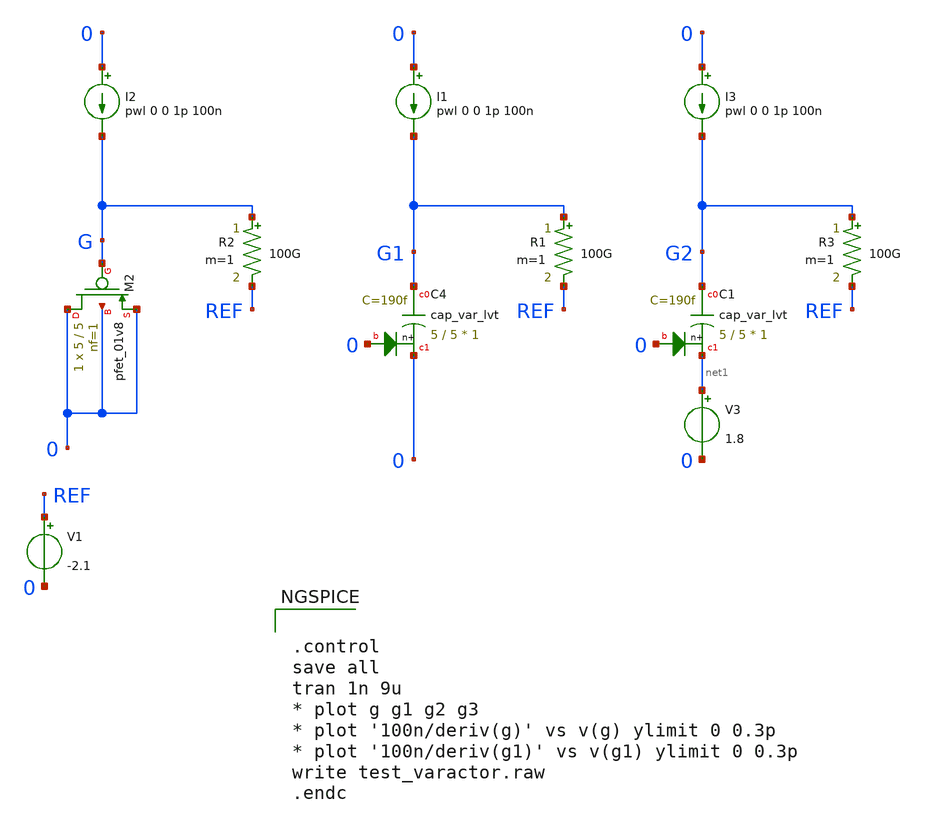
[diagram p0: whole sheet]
** sch_path: sky130A/xschem_libs/sky130_tests/test_varactor/schematic/test_varactor.sch
* Copyright 2021 Stefan Frederik Schippers
* Licensed under the Apache License, Version 2.0 (the "License");
* you may not use this file except in compliance with the License.
* You may obtain a copy of the License at
* https://www.apache.org/licenses/LICENSE-2.0
* Unless required by applicable law or agreed to in writing, software
* distributed under the License is distributed on an "AS IS" BASIS,
* WITHOUT WARRANTIES OR CONDITIONS OF ANY KIND, either express or implied.
* See the License for the specific language governing permissions and
* limitations under the License.
**.subckt test_varactor
I1 0 G1 pwl 0 0 1p 100n
R1 G1 REF 100G m=1
I2 0 G pwl 0 0 1p 100n
R2 G REF 100G m=1
V1 REF 0 -2.1
XC4 G1 0 0 sky130_fd_pr__cap_var_lvt W=5 L=5 VM=1 m=1
XM2 0 G 0 0 sky130_fd_pr__pfet_01v8 L=5 W=5 nf=1 ad='int((nf+1)/2) * W/nf * 0.29' as='int((nf+2)/2) * W/nf * 0.29'
+ pd='2*int((nf+1)/2) * (W/nf + 0.29)' ps='2*int((nf+2)/2) * (W/nf + 0.29)' nrd='0.29 / W' nrs='0.29 / W'
+ sa=0 sb=0 sd=0 mult=1 m=1
I3 0 G2 pwl 0 0 1p 100n
R3 G2 REF 100G m=1
XC1 G2 net1 0 sky130_fd_pr__cap_var_lvt W=5 L=5 VM=1 m=1
V3 net1 0 1.8
**** begin user architecture code


.control
save all
tran 1n 9u
* plot g g1 g2 g3
* plot '100n/deriv(g)' vs v(g) ylimit 0 0.3p
* plot '100n/deriv(g1)' vs v(g1) ylimit 0 0.3p
write test_varactor.raw
.endc



** opencircuitdesign pdks install
.lib $::SKYWATER_MODELS/sky130.lib.spice tt

**** end user architecture code
**.ends
.end
